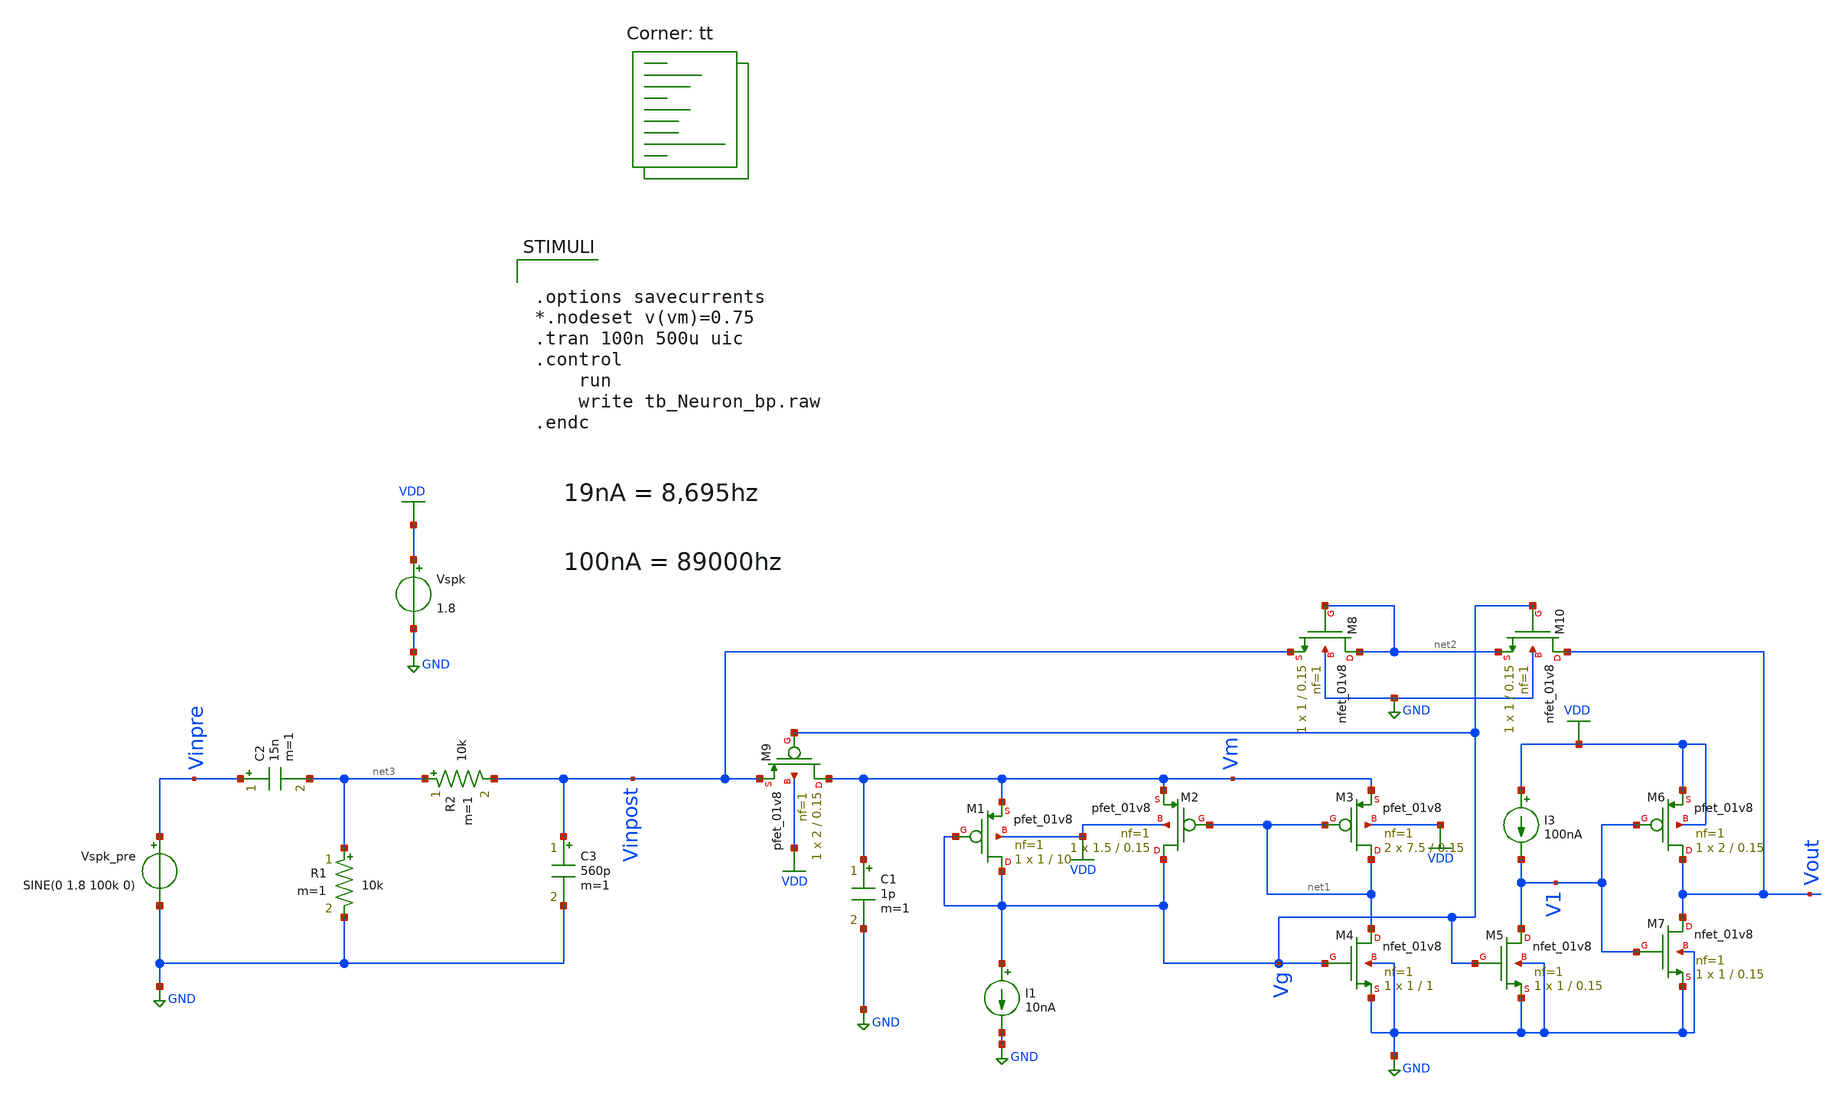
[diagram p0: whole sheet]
** sch_path: Neuron/ultralif/tb_Neuron_bp.sch
**.subckt tb_Neuron_bp
XM1 Vg Vg Vm VDD sky130_fd_pr__pfet_01v8 L=10 W=1 nf=1 ad='int((nf+1)/2) * W/nf * 0.29' as='int((nf+2)/2) * W/nf * 0.29'
+ pd='2*int((nf+1)/2) * (W/nf + 0.29)' ps='2*int((nf+2)/2) * (W/nf + 0.29)' nrd='0.29 / W' nrs='0.29 / W'
+ sa=0 sb=0 sd=0 mult=1 m=1
XM2 Vg net1 Vm VDD sky130_fd_pr__pfet_01v8 L=0.15 W=1.5 nf=1 ad='int((nf+1)/2) * W/nf * 0.29' as='int((nf+2)/2) * W/nf * 0.29'
+ pd='2*int((nf+1)/2) * (W/nf + 0.29)' ps='2*int((nf+2)/2) * (W/nf + 0.29)' nrd='0.29 / W' nrs='0.29 / W'
+ sa=0 sb=0 sd=0 mult=1 m=1
XM3 net1 net1 Vm VDD sky130_fd_pr__pfet_01v8 L=0.15 W=7.5 nf=1 ad='int((nf+1)/2) * W/nf * 0.29' as='int((nf+2)/2) * W/nf * 0.29'
+ pd='2*int((nf+1)/2) * (W/nf + 0.29)' ps='2*int((nf+2)/2) * (W/nf + 0.29)' nrd='0.29 / W' nrs='0.29 / W'
+ sa=0 sb=0 sd=0 mult=2 m=2
XM4 net1 Vg GND GND sky130_fd_pr__nfet_01v8 L=1 W=1 nf=1 ad='int((1 + 1)/2) * 1 / 1 * 0.29' as='int((1 + 2)/2) * 1 / 1 * 0.29'
+ pd='2*int((1 + 1)/2) * (1 / 1 + 0.29)' ps='2*int((1 + 2)/2) * (1 / 1 + 0.29)' nrd='0.29 / 1 ' nrs='0.29 / 1 '
+ sa=0 sb=0 sd=0 mult=1 m=1
XM5 V1 Vg GND GND sky130_fd_pr__nfet_01v8 L=0.15 W=1 nf=1 ad='int((1 + 1)/2) * 1 / 1 * 0.29' as='int((1 + 2)/2) * 1 / 1 * 0.29'
+ pd='2*int((1 + 1)/2) * (1 / 1 + 0.29)' ps='2*int((1 + 2)/2) * (1 / 1 + 0.29)' nrd='0.29 / 1 ' nrs='0.29 / 1 '
+ sa=0 sb=0 sd=0 mult=1 m=1
XM6 Vout V1 VDD VDD sky130_fd_pr__pfet_01v8 L=0.15 W=2 nf=1 ad='int((nf+1)/2) * W/nf * 0.29' as='int((nf+2)/2) * W/nf * 0.29'
+ pd='2*int((nf+1)/2) * (W/nf + 0.29)' ps='2*int((nf+2)/2) * (W/nf + 0.29)' nrd='0.29 / W' nrs='0.29 / W'
+ sa=0 sb=0 sd=0 mult=1 m=1
XM7 Vout V1 GND GND sky130_fd_pr__nfet_01v8 L=0.15 W=1 nf=1 ad='int((1 + 1)/2) * 1 / 1 * 0.29' as='int((1 + 2)/2) * 1 / 1 * 0.29'
+ pd='2*int((1 + 1)/2) * (1 / 1 + 0.29)' ps='2*int((1 + 2)/2) * (1 / 1 + 0.29)' nrd='0.29 / 1 ' nrs='0.29 / 1 '
+ sa=0 sb=0 sd=0 mult=1 m=1
I1 Vg GND 10nA
Vspk VDD GND 1.8
C1 Vm GND 1p m=1
I3 VDD V1 100nA
XM8 net2 net2 Vinpost GND sky130_fd_pr__nfet_01v8 L=0.15 W=1 nf=1 ad='int((1 + 1)/2) * 1 / 1 * 0.29'
+ as='int((1 + 2)/2) * 1 / 1 * 0.29' pd='2*int((1 + 1)/2) * (1 / 1 + 0.29)' ps='2*int((1 + 2)/2) * (1 / 1 + 0.29)'
+ nrd='0.29 / 1 ' nrs='0.29 / 1 ' sa=0 sb=0 sd=0 mult=1 m=1
XM9 Vm Vg Vinpost VDD sky130_fd_pr__pfet_01v8 L=0.15 W=2 nf=1 ad='int((nf+1)/2) * W/nf * 0.29' as='int((nf+2)/2) * W/nf * 0.29'
+ pd='2*int((nf+1)/2) * (W/nf + 0.29)' ps='2*int((nf+2)/2) * (W/nf + 0.29)' nrd='0.29 / W' nrs='0.29 / W'
+ sa=0 sb=0 sd=0 mult=1 m=1
R1 net3 GND 10k m=1
R2 net3 Vinpost 10k m=1
C2 Vinpre net3 15n m=1
Vspk_pre Vinpre GND SINE(0 1.8 100k 0)
C3 Vinpost GND 560p m=1
XM10 Vout Vg net2 GND sky130_fd_pr__nfet_01v8 L=0.15 W=1 nf=1 ad='int((1 + 1)/2) * 1 / 1 * 0.29' as='int((1 + 2)/2) * 1 / 1 * 0.29'
+ pd='2*int((1 + 1)/2) * (1 / 1 + 0.29)' ps='2*int((1 + 2)/2) * (1 / 1 + 0.29)' nrd='0.29 / 1 ' nrs='0.29 / 1 '
+ sa=0 sb=0 sd=0 mult=1 m=1
**** begin user architecture code
.lib $::SKYWATER_MODELS/sky130.lib.spice tt
**** end user architecture code
**.ends
.GLOBAL GND
.GLOBAL VDD
**** begin user architecture code


.options savecurrents
*.nodeset v(vm)=0.75
.tran 100n 500u uic
.control
	run
	write tb_Neuron_bp.raw
.endc


**** end user architecture code
.end
